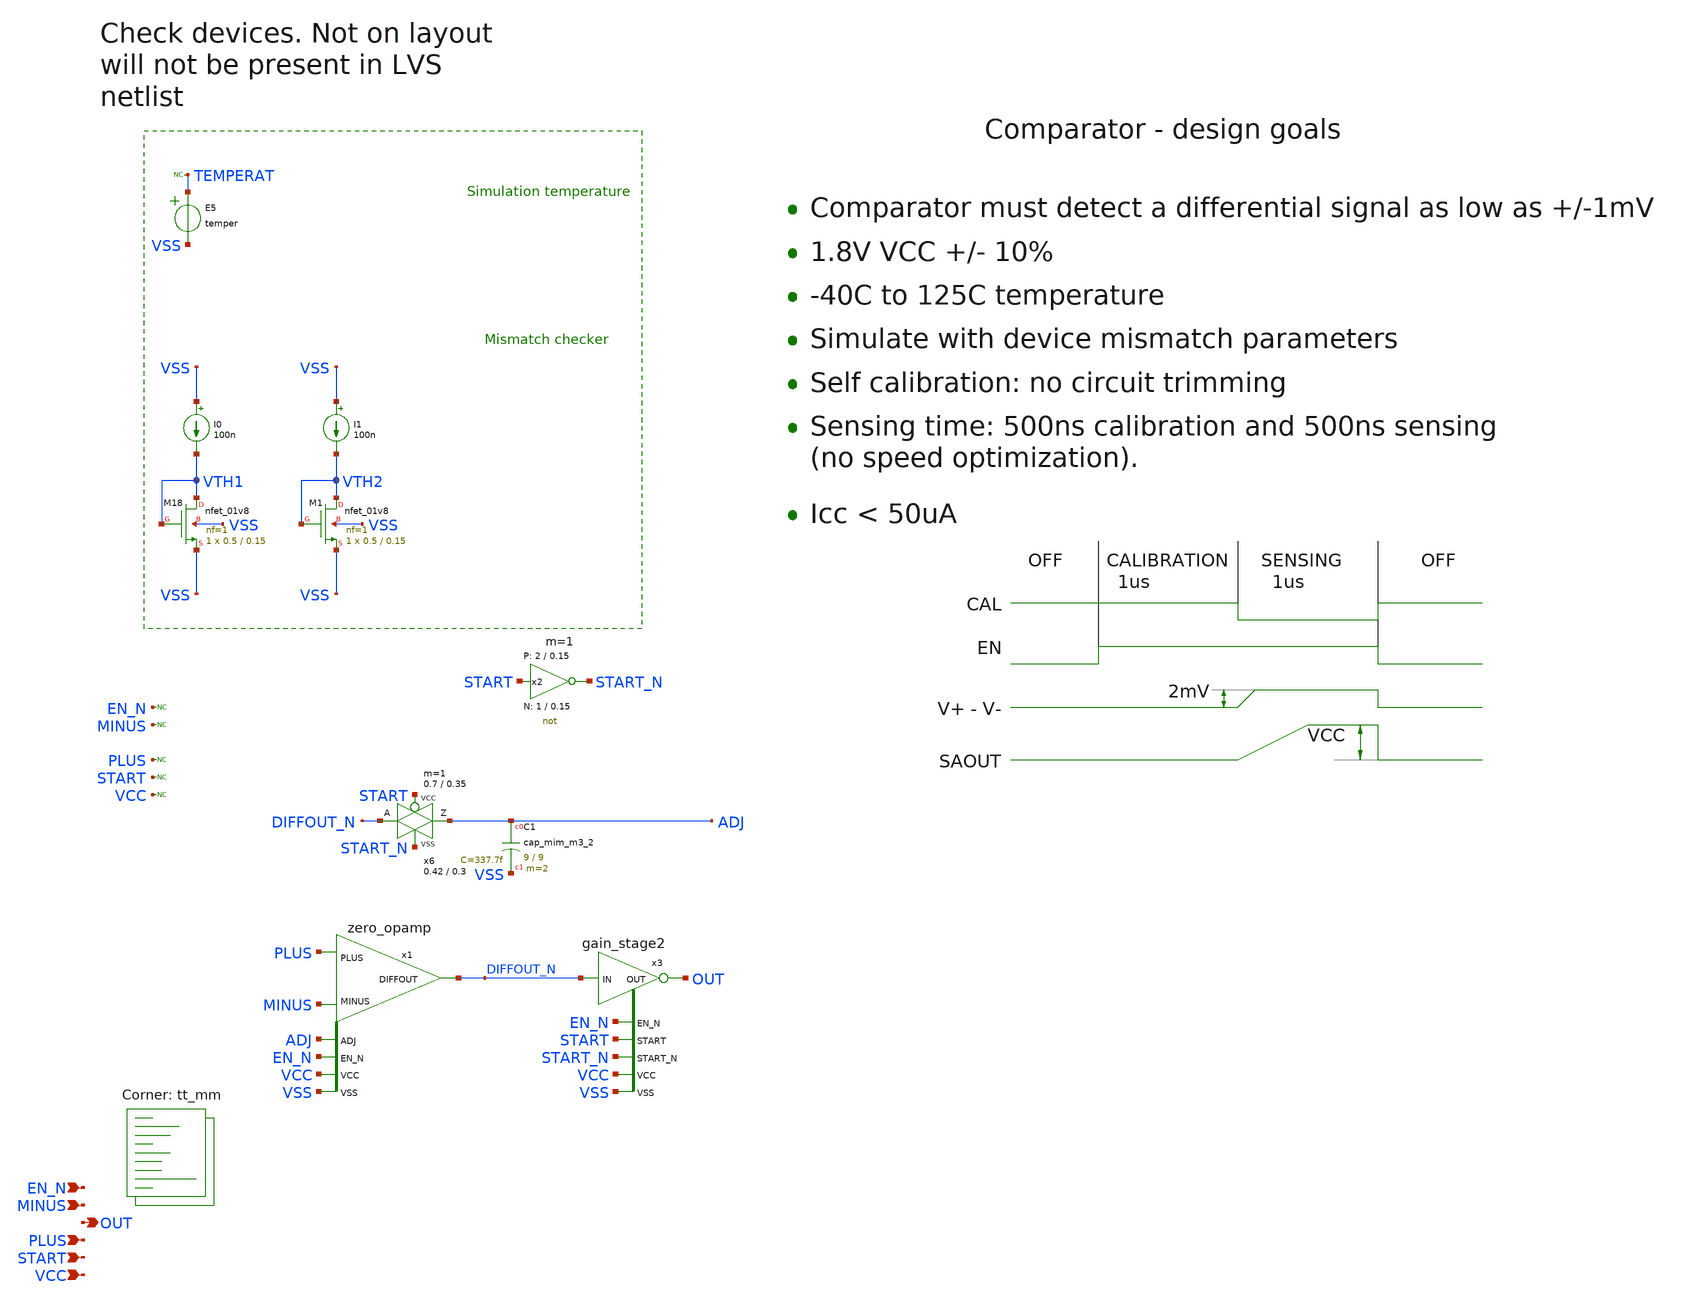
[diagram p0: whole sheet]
** sch_path: sky130A/xschem_libs/sky130_tests/tb_bandgap_opamp/schematic/tb_bandgap_opamp.sch
* Copyright 2021 Stefan Frederik Schippers
* Licensed under the Apache License, Version 2.0 (the "License");
* you may not use this file except in compliance with the License.
* You may obtain a copy of the License at
* https://www.apache.org/licenses/LICENSE-2.0
* Unless required by applicable law or agreed to in writing, software
* distributed under the License is distributed on an "AS IS" BASIS,
* WITHOUT WARRANTIES OR CONDITIONS OF ANY KIND, either express or implied.
* See the License for the specific language governing permissions and
* limitations under the License.
**.subckt tb_bandgap_opamp VCC START PLUS OUT MINUS EN_N
*.ipin VCC
*.ipin START
*.ipin PLUS
*.opin OUT
*.ipin MINUS
*.ipin EN_N
x6 ADJ DIFFOUT_N START START_N VCC VSS passgate_1 W_N=0.42 L_N=0.3 W_P=0.7 L_P=0.35 m=1
XC1 ADJ VSS sky130_fd_pr__cap_mim_m3_2 W=9 L=9 MF=2 m=2
x2 START_N START VCC VSS not W_N=1 L_N=0.15 W_P=2 L_P=0.15 m=1
x1 EN_N MINUS PLUS DIFFOUT_N VCC VSS ADJ zero_opamp
XM18 VTH1 VTH1 VSS VSS sky130_fd_pr__nfet_01v8 L=0.15 W=0.5 nf=1 ad='int((1 + 1)/2) * 0.5 / 1 * 0.29'
+ as='int((1 + 2)/2) * 0.5 / 1 * 0.29' pd='2*int((1 + 1)/2) * (0.5 / 1 + 0.29)' ps='2*int((1 + 2)/2) * (0.5 / 1 + 0.29)'
+ nrd='0.29 / 0.5 ' nrs='0.29 / 0.5 ' sa=0 sb=0 sd=0 mult=1 m=1
I0 VSS VTH1 100n
x3 DIFFOUT_N OUT VCC VSS START_N START EN_N gain_stage2 WN=0.5 WP=1 wcap=9
E5 TEMPERAT VSS VOL=' temper '
* noconn TEMPERAT
* noconn EN_N
* noconn MINUS
* noconn PLUS
* noconn START
* noconn VCC
XM1 VTH2 VTH2 VSS VSS sky130_fd_pr__nfet_01v8 L=0.15 W=0.5 nf=1 ad='int((1 + 1)/2) * 0.5 / 1 * 0.29'
+ as='int((1 + 2)/2) * 0.5 / 1 * 0.29' pd='2*int((1 + 1)/2) * (0.5 / 1 + 0.29)' ps='2*int((1 + 2)/2) * (0.5 / 1 + 0.29)'
+ nrd='0.29 / 0.5 ' nrs='0.29 / 0.5 ' sa=0 sb=0 sd=0 mult=1 m=1
I1 VSS VTH2 100n
**** begin user architecture code
.lib $::SKYWATER_MODELS/sky130.lib.spice tt_mm
**** end user architecture code
**.ends
**** begin user architecture code

* .option SCALE=1e-6
.option method=gear
.option savecurrents

* this experimental option enables mos model bin
* selection based on W/NF instead of W
.option wnflag=1


.param VCCGAUSS = agauss(1.8, 0.05, 1)
.param VCC = 'VCCGAUSS'
** use following line to remove VCC variations
* .param VCC = 1.8

.param TEMPGAUSS = agauss(40, 30, 1)
.option temp = 'TEMPGAUSS'
** use following line to remove temperature variations
* .option temp = 25

.include stimuli_tb_bandgap_opamp.cir
.control
  setseed 11
  reset
  let run=0
  dowhile run <= 100
    save all
    tran 1n 2500n uic
    print run
    print @m.x1.xml.msky130_fd_pr__pfet_01v8_lvt[vth]
    print @m.x1.xmr.msky130_fd_pr__pfet_01v8_lvt[vth]

    remzerovec
    write tb_bandgap_opamp.raw
    set appendwrite
    reset
    let run = run + 1
  end
.endc


**** end user architecture code
.end
